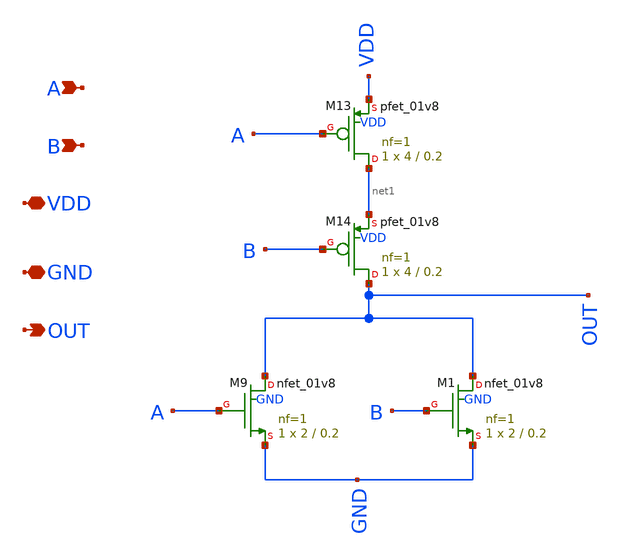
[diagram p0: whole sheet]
** sch_path: pll/pfd_cp_lf_lib/coventional_pfd/xschem/Nor_gate.sch
**.subckt Nor_gate A B VDD GND OUT
*.ipin A
*.ipin B
*.iopin VDD
*.iopin GND
*.opin OUT
XM9 OUT A GND GND sky130_fd_pr__nfet_01v8 L=0.2 W=2 nf=1 ad='int((nf+1)/2) * W/nf * 0.29' as='int((nf+2)/2) * W/nf * 0.29'
+ pd='2*int((nf+1)/2) * (W/nf + 0.29)' ps='2*int((nf+2)/2) * (W/nf + 0.29)' nrd='0.29 / W' nrs='0.29 / W'
+ sa=0 sb=0 sd=0 mult=1 m=1
XM1 OUT B GND GND sky130_fd_pr__nfet_01v8 L=0.2 W=2 nf=1 ad='int((nf+1)/2) * W/nf * 0.29' as='int((nf+2)/2) * W/nf * 0.29'
+ pd='2*int((nf+1)/2) * (W/nf + 0.29)' ps='2*int((nf+2)/2) * (W/nf + 0.29)' nrd='0.29 / W' nrs='0.29 / W'
+ sa=0 sb=0 sd=0 mult=1 m=1
XM13 net1 A VDD VDD sky130_fd_pr__pfet_01v8 L=0.2 W=4 nf=1 ad='int((nf+1)/2) * W/nf * 0.29' as='int((nf+2)/2) * W/nf * 0.29'
+ pd='2*int((nf+1)/2) * (W/nf + 0.29)' ps='2*int((nf+2)/2) * (W/nf + 0.29)' nrd='0.29 / W' nrs='0.29 / W'
+ sa=0 sb=0 sd=0 mult=1 m=1
XM14 OUT B net1 VDD sky130_fd_pr__pfet_01v8 L=0.2 W=4 nf=1 ad='int((nf+1)/2) * W/nf * 0.29' as='int((nf+2)/2) * W/nf * 0.29'
+ pd='2*int((nf+1)/2) * (W/nf + 0.29)' ps='2*int((nf+2)/2) * (W/nf + 0.29)' nrd='0.29 / W' nrs='0.29 / W'
+ sa=0 sb=0 sd=0 mult=1 m=1
**.ends
.end
